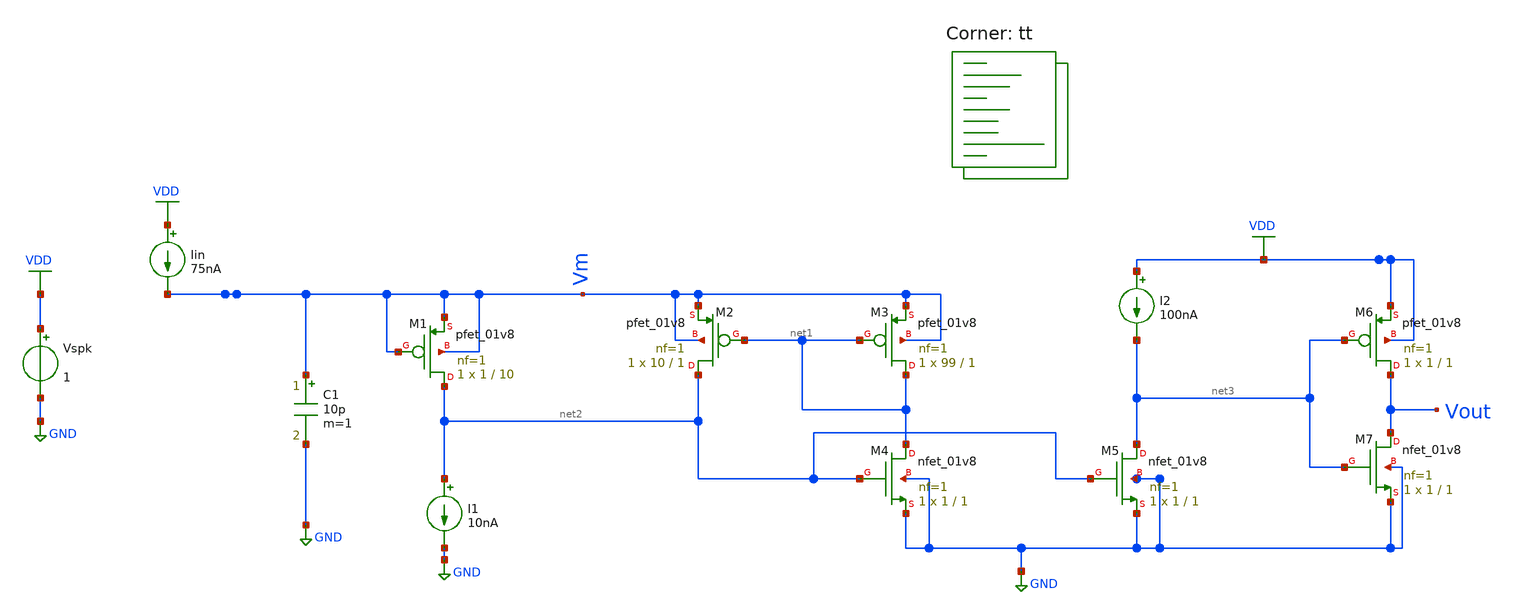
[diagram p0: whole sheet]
** sch_path: Schematics/Neurona_Simulacion.sch
**.subckt Neurona_Simulacion
XM1 net2 Vm Vm Vm sky130_fd_pr__pfet_01v8 L=10 W=1 nf=1 ad='int((nf+1)/2) * W/nf * 0.29' as='int((nf+2)/2) * W/nf * 0.29'
+ pd='2*int((nf+1)/2) * (W/nf + 0.29)' ps='2*int((nf+2)/2) * (W/nf + 0.29)' nrd='0.29 / W' nrs='0.29 / W'
+ sa=0 sb=0 sd=0 mult=1 m=1
XM2 net2 net1 Vm Vm sky130_fd_pr__pfet_01v8 L=1 W=10 nf=1 ad='int((nf+1)/2) * W/nf * 0.29' as='int((nf+2)/2) * W/nf * 0.29'
+ pd='2*int((nf+1)/2) * (W/nf + 0.29)' ps='2*int((nf+2)/2) * (W/nf + 0.29)' nrd='0.29 / W' nrs='0.29 / W'
+ sa=0 sb=0 sd=0 mult=1 m=1
XM3 net1 net1 Vm Vm sky130_fd_pr__pfet_01v8 L=1 W=99 nf=1 ad='int((nf+1)/2) * W/nf * 0.29' as='int((nf+2)/2) * W/nf * 0.29'
+ pd='2*int((nf+1)/2) * (W/nf + 0.29)' ps='2*int((nf+2)/2) * (W/nf + 0.29)' nrd='0.29 / W' nrs='0.29 / W'
+ sa=0 sb=0 sd=0 mult=1 m=1
XM4 net1 net2 GND GND sky130_fd_pr__nfet_01v8 L=1 W=1 nf=1 ad='int((1 + 1)/2) * 1 / 1 * 0.29' as='int((1 + 2)/2) * 1 / 1 * 0.29'
+ pd='2*int((1 + 1)/2) * (1 / 1 + 0.29)' ps='2*int((1 + 2)/2) * (1 / 1 + 0.29)' nrd='0.29 / 1 ' nrs='0.29 / 1 '
+ sa=0 sb=0 sd=0 mult=1 m=1
XM5 net3 net2 GND GND sky130_fd_pr__nfet_01v8 L=1 W=1 nf=1 ad='int((1 + 1)/2) * 1 / 1 * 0.29' as='int((1 + 2)/2) * 1 / 1 * 0.29'
+ pd='2*int((1 + 1)/2) * (1 / 1 + 0.29)' ps='2*int((1 + 2)/2) * (1 / 1 + 0.29)' nrd='0.29 / 1 ' nrs='0.29 / 1 '
+ sa=0 sb=0 sd=0 mult=1 m=1
XM6 Vout net3 VDD VDD sky130_fd_pr__pfet_01v8 L=1 W=1 nf=1 ad='int((nf+1)/2) * W/nf * 0.29' as='int((nf+2)/2) * W/nf * 0.29'
+ pd='2*int((nf+1)/2) * (W/nf + 0.29)' ps='2*int((nf+2)/2) * (W/nf + 0.29)' nrd='0.29 / W' nrs='0.29 / W'
+ sa=0 sb=0 sd=0 mult=1 m=1
XM7 Vout net3 GND GND sky130_fd_pr__nfet_01v8 L=1 W=1 nf=1 ad='int((1 + 1)/2) * 1 / 1 * 0.29' as='int((1 + 2)/2) * 1 / 1 * 0.29'
+ pd='2*int((1 + 1)/2) * (1 / 1 + 0.29)' ps='2*int((1 + 2)/2) * (1 / 1 + 0.29)' nrd='0.29 / 1 ' nrs='0.29 / 1 '
+ sa=0 sb=0 sd=0 mult=1 m=1
I2 VDD net3 100nA
I1 net2 GND 10nA
Vspk VDD GND 1
C1 Vm GND 10p m=1
Iin VDD Vm 75nA
**** begin user architecture code
.lib $::SKYWATER_MODELS/sky130.lib.spice tt
**** end user architecture code
**.ends
.GLOBAL GND
.GLOBAL VDD
**** begin user architecture code

.options savecurrents
.tran 100n 10m uic
.save all
.control
	run
	write Neurona_Simulacion.raw
*plot all.Vout
.endc


**** end user architecture code
.end
